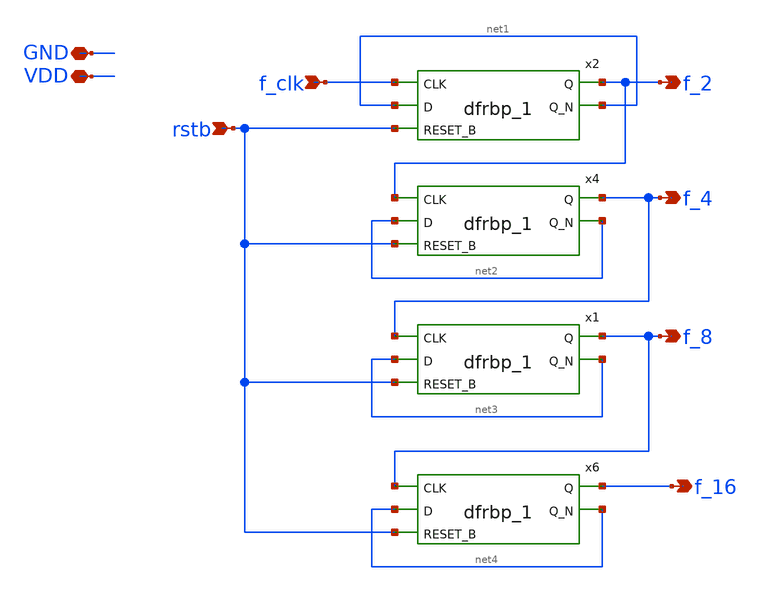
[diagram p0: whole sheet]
** sch_path: xschem/readout/fclk_tree.sch
**.subckt fclk_tree VDD GND rstb f_2 f_4 f_8 f_16 f_clk
*.iopin VDD
*.iopin GND
*.ipin rstb
*.opin f_2
*.opin f_4
*.opin f_8
*.opin f_16
*.ipin f_clk
x2 f_clk net1 rstb gnd gnd vdd vdd f_2 net1 sky130_fd_sc_lp__dfrbp_1
x4 f_2 net2 rstb gnd gnd vdd vdd f_4 net2 sky130_fd_sc_lp__dfrbp_1
x1 f_4 net3 rstb gnd gnd vdd vdd f_8 net3 sky130_fd_sc_lp__dfrbp_1
x6 f_8 net4 rstb gnd gnd vdd vdd f_16 net4 sky130_fd_sc_lp__dfrbp_1
**.ends
.end
